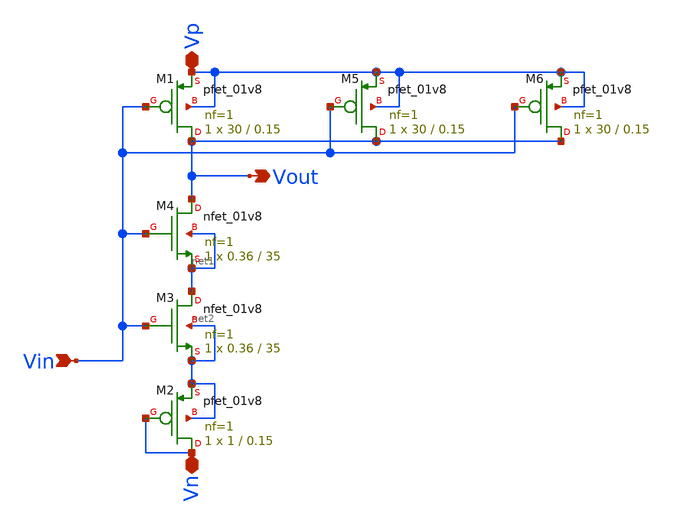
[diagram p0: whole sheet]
** sch_path: xschem/Vth_sch/Symbol/Inverter-th15.sch
**.subckt Inverter-th15 Vin Vout Vn Vp
*.ipin Vin
*.opin Vout
*.iopin Vn
*.iopin Vp
XM1 Vout Vin Vp Vp sky130_fd_pr__pfet_01v8 L=0.15 W=30 nf=1 ad='int((nf+1)/2) * W/nf * 0.29' as='int((nf+2)/2) * W/nf * 0.29'
+ pd='2*int((nf+1)/2) * (W/nf + 0.29)' ps='2*int((nf+2)/2) * (W/nf + 0.29)' nrd='0.29 / W' nrs='0.29 / W'
+ sa=0 sb=0 sd=0 mult=1 m=1
XM3 net1 Vin net2 net2 sky130_fd_pr__nfet_01v8 L=35 W=0.36 nf=1 ad='int((nf+1)/2) * W/nf * 0.29' as='int((nf+2)/2) * W/nf * 0.29'
+ pd='2*int((nf+1)/2) * (W/nf + 0.29)' ps='2*int((nf+2)/2) * (W/nf + 0.29)' nrd='0.29 / W' nrs='0.29 / W'
+ sa=0 sb=0 sd=0 mult=1 m=1
XM4 Vout Vin net1 net1 sky130_fd_pr__nfet_01v8 L=35 W=0.36 nf=1 ad='int((nf+1)/2) * W/nf * 0.29' as='int((nf+2)/2) * W/nf * 0.29'
+ pd='2*int((nf+1)/2) * (W/nf + 0.29)' ps='2*int((nf+2)/2) * (W/nf + 0.29)' nrd='0.29 / W' nrs='0.29 / W'
+ sa=0 sb=0 sd=0 mult=1 m=1
XM5 Vout Vin Vp Vp sky130_fd_pr__pfet_01v8 L=0.15 W=30 nf=1 ad='int((nf+1)/2) * W/nf * 0.29' as='int((nf+2)/2) * W/nf * 0.29'
+ pd='2*int((nf+1)/2) * (W/nf + 0.29)' ps='2*int((nf+2)/2) * (W/nf + 0.29)' nrd='0.29 / W' nrs='0.29 / W'
+ sa=0 sb=0 sd=0 mult=1 m=1
XM6 Vout Vin Vp Vp sky130_fd_pr__pfet_01v8 L=0.15 W=30 nf=1 ad='int((nf+1)/2) * W/nf * 0.29' as='int((nf+2)/2) * W/nf * 0.29'
+ pd='2*int((nf+1)/2) * (W/nf + 0.29)' ps='2*int((nf+2)/2) * (W/nf + 0.29)' nrd='0.29 / W' nrs='0.29 / W'
+ sa=0 sb=0 sd=0 mult=1 m=1
XM2 Vn Vn net2 net2 sky130_fd_pr__pfet_01v8 L=0.15 W=1 nf=1 ad='int((nf+1)/2) * W/nf * 0.29' as='int((nf+2)/2) * W/nf * 0.29'
+ pd='2*int((nf+1)/2) * (W/nf + 0.29)' ps='2*int((nf+2)/2) * (W/nf + 0.29)' nrd='0.29 / W' nrs='0.29 / W'
+ sa=0 sb=0 sd=0 mult=1 m=1
**.ends
.end
